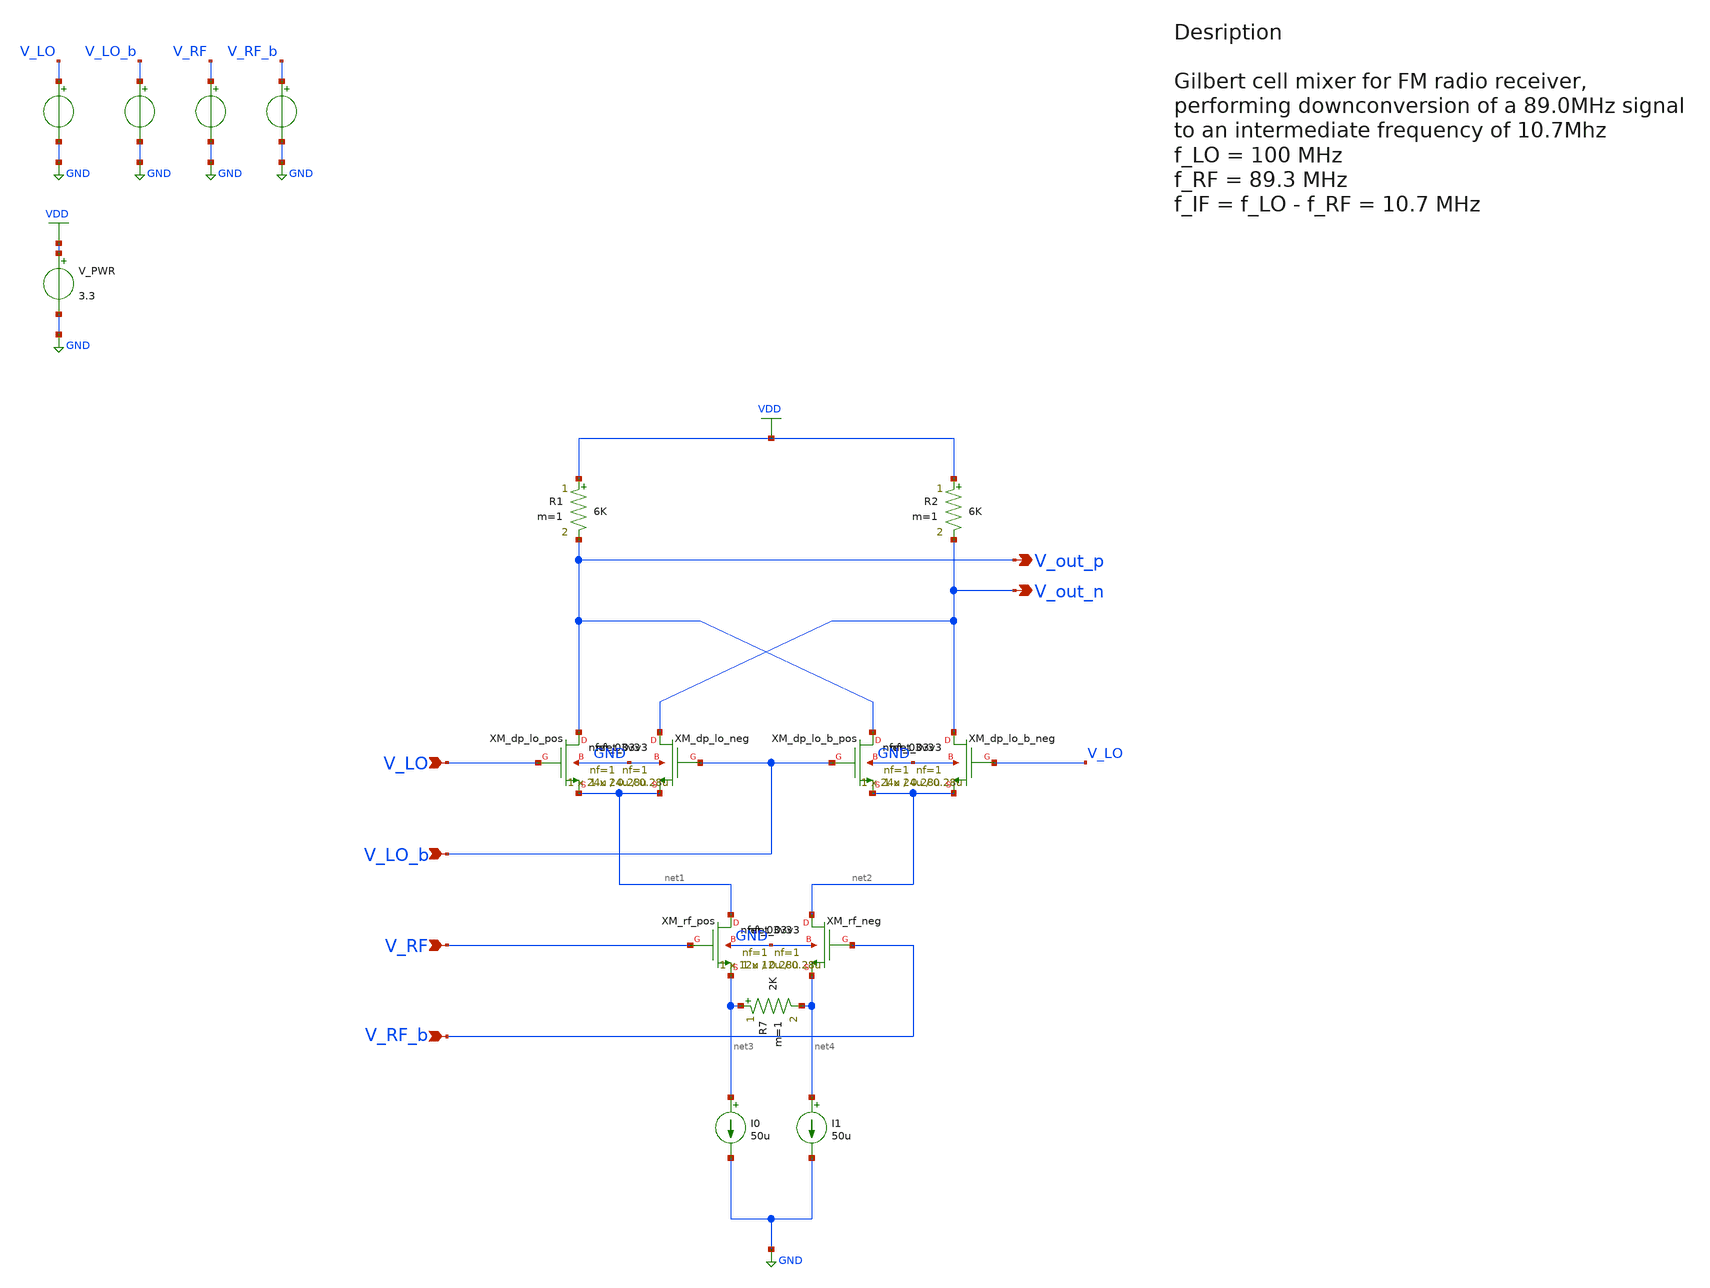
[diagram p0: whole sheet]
** sch_path: src/design_xsch/Gilbert_cell_no_hierarchy.sch
**.subckt Gilbert_cell_no_hierarchy V_LO V_LO_b V_RF V_RF_b V_out_p V_out_n
*.ipin V_LO
*.ipin V_LO_b
*.ipin V_RF
*.ipin V_RF_b
*.opin V_out_p
*.opin V_out_n
R1 VDD V_out_p 6K m=1
R2 VDD V_out_n 6K m=1
V_PWR VDD GND 3.3
.save i(v_pwr)
V_LO V_LO GND pulse(0 1.5 0 1p 1p 0.25n 0.5n)
.save i(v_lo)
V_LO_b V_LO_b GND pulse(0 1.5 0 1p 1p 0.25n 0.5n)
.save i(v_lo_b)
V_RF V_RF GND sin( 1 1 1 0 )
.save i(v_rf)
V_RF_b V_RF_b GND sin( 1 1 1 0 0 180 )
.save i(v_rf_b)
I0 net3 GND 50u
I1 net4 GND 50u
XM_dp_lo_pos V_out_p V_LO net1 GND nfet_03v3 L=0.28u W=24u nf=1 ad='int((nf+1)/2) * W/nf * 0.18u' as='int((nf+2)/2) * W/nf * 0.18u'
+ pd='2*int((nf+1)/2) * (W/nf + 0.18u)' ps='2*int((nf+2)/2) * (W/nf + 0.18u)' nrd='0.18u / W' nrs='0.18u / W'
+ sa=0 sb=0 sd=0 m=1
XM_dp_lo_neg V_out_n V_LO_b net1 GND nfet_03v3 L=0.28u W=24u nf=1 ad='int((nf+1)/2) * W/nf * 0.18u' as='int((nf+2)/2) * W/nf * 0.18u'
+ pd='2*int((nf+1)/2) * (W/nf + 0.18u)' ps='2*int((nf+2)/2) * (W/nf + 0.18u)' nrd='0.18u / W' nrs='0.18u / W'
+ sa=0 sb=0 sd=0 m=1
XM_dp_lo_b_pos V_out_p V_LO_b net2 GND nfet_03v3 L=0.28u W=24u nf=1 ad='int((nf+1)/2) * W/nf * 0.18u'
+ as='int((nf+2)/2) * W/nf * 0.18u' pd='2*int((nf+1)/2) * (W/nf + 0.18u)' ps='2*int((nf+2)/2) * (W/nf + 0.18u)'
+ nrd='0.18u / W' nrs='0.18u / W' sa=0 sb=0 sd=0 m=1
XM_dp_lo_b_neg V_out_n V_LO net2 GND nfet_03v3 L=0.28u W=24u nf=1 ad='int((nf+1)/2) * W/nf * 0.18u' as='int((nf+2)/2) * W/nf * 0.18u'
+ pd='2*int((nf+1)/2) * (W/nf + 0.18u)' ps='2*int((nf+2)/2) * (W/nf + 0.18u)' nrd='0.18u / W' nrs='0.18u / W'
+ sa=0 sb=0 sd=0 m=1
XM_rf_pos net1 V_RF net3 GND nfet_03v3 L=0.28u W=12u nf=1 ad='int((nf+1)/2) * W/nf * 0.18u' as='int((nf+2)/2) * W/nf * 0.18u'
+ pd='2*int((nf+1)/2) * (W/nf + 0.18u)' ps='2*int((nf+2)/2) * (W/nf + 0.18u)' nrd='0.18u / W' nrs='0.18u / W'
+ sa=0 sb=0 sd=0 m=1
XM_rf_neg net2 V_RF_b net4 GND nfet_03v3 L=0.28u W=12u nf=1 ad='int((nf+1)/2) * W/nf * 0.18u' as='int((nf+2)/2) * W/nf * 0.18u'
+ pd='2*int((nf+1)/2) * (W/nf + 0.18u)' ps='2*int((nf+2)/2) * (W/nf + 0.18u)' nrd='0.18u / W' nrs='0.18u / W'
+ sa=0 sb=0 sd=0 m=1
R7 net3 net4 2K m=1
**** begin user architecture code

.include $::180MCU_MODELS/design.ngspice
.lib $::180MCU_MODELS/sm141064.ngspice typical
.lib $::180MCU_MODELS/sm141064.ngspice mimcap_typical
.lib $::180MCU_MODELS/sm141064.ngspice cap_mim
.lib $::180MCU_MODELS/sm141064.ngspice res_typical




* let sets vectors to a plot, while set sets a variable, globally accessible in .control
.control

    * Set frequency and amplitude variables to proper values from within the control sequence
    * sine-wave LO
    * set cm_lo = 0.5
    * set freq_lo = 2.50G
    * set amp_lo = 0.5
    * alter @V_LO[sin] = [ $cm_lo $amp_lo $freq_lo 0 ]
    * alter @V_LO_b[sin] = [ $cm_lo $amp_lo $freq_lo 0 0 180 ]

    set freq_lo = 100Meg
    set cm_lo = 1.8
    set amp_lo = 0.25

    set cm_rf  = 1,6
    set freq_rf = 89.3Meg
    set amp_rf  = 0.2

    * set the parameters to the voltage sources
    * alter @V_LO[pulse] = [ 2 2.5 0 0.5p 0.5p 5n 10n ]
    * alter @V_LO_b[pulse] = [ 2 2.5 5n 0.5p 0.5p 5n 10n]
    alter @V_LO[sin] = [ $cm_lo $amp_lo $freq_lo 0 ]
    alter @V_LO_b[sin] = [ $cm_lo $amp_lo $freq_lo 0 0 180 ]
    alter @V_RF[sin] = [ $cm_rf $amp_rf $freq_rf 0 ]
    alter @V_RF_b[sin] = [ $cm_rf $amp_rf $freq_rf 0 0 180 ]

    save all

    * operating point
    op
    show

    * save transistor op parameters
    * diff_pair_1 transistors
    save @m.xm_rf_pos.m0[vgs]
    save @m.xm_rf_pos.m0[vds]
    save @m.xm_rf_pos.m0[id]
    save @m.xm_rf_pos.m0[gm]
    save @m.xm_rf_pos.m0[vth]
    save @m.xm_rf_pos.m0[cgg]
    save @m.xm_rf_neg.m0[vgs]
    save @m.xm_rf_neg.m0[vds]
    save @m.xm_rf_neg.m0[id]
    save @m.xm_rf_neg.m0[gm]
    save @m.xm_rf_neg.m0[vth]
    save @m.xm_rf_neg.m0[cgg]

    * diff_pair_2 transistors
    * save @m.xdiff_pair_2.xm1.m0[vgs]
    * save @m.xdiff_pair_2.xm1.m0[vds]
    * save @m.xdiff_pair_2.xm1.m0[id]
    * save @m.xdiff_pair_2.xm1.m0[gm]
    * save @m.xdiff_pair_2.xm1.m0[vth]
    * save @m.xdiff_pair_2.xm1.m0[cgg]
    * save @m.xdiff_pair_2.xm2.m0[vgs]
    * save @m.xdiff_pair_2.xm2.m0[vds]
    * save @m.xdiff_pair_2.xm2.m0[id]
    * save @m.xdiff_pair_2.xm2.m0[gm]
    * save @m.xdiff_pair_2.xm2.m0[vth]
    * save @m.xdiff_pair_2.xm2.m0[cgg]

    * diff_pair_3 transistors
    * save @m.xdiff_pair_3.xm1.m0[vgs]
    * save @m.xdiff_pair_3.xm1.m0[vds]
    * save @m.xdiff_pair_3.xm1.m0[id]
    * save @m.xdiff_pair_3.xm1.m0[gm]
    * save @m.xdiff_pair_3.xm1.m0[vth]
    * save @m.xdiff_pair_3.xm1.m0[cgg]
    * save @m.xdiff_pair_3.xm2.m0[vgs]
    * save @m.xdiff_pair_3.xm2.m0[vds]
    * save @m.xdiff_pair_3.xm2.m0[id]
    * save @m.xdiff_pair_3.xm2.m0[gm]
    * save @m.xdiff_pair_3.xm2.m0[vth]
    * save @m.xdiff_pair_3.xm2.m0[cgg]

    write Gilbert_no_hierarchy_sim.raw

    set appendwrite

    * Transient analysis to observe mixing operation
    tran 1p 300n
    write Gilbert_no_hierarchy_sim.raw

    * Calculate differential output for conversion gain measurement
    let v_out_diff = v(v_out_p)-v(v_out_n)
    let v_rf_diff = v(v_rf)-v(v_rf_b)

    * Extract IF component at 100MHz using FFT
    linearize v_out_diff v_rf_diff
    let time_step = 10e-12
    let sample_freq = 1/time_step
    let npts = length(v_out_diff)
    let freq_res = sample_freq/npts


    fft v_out_diff v_rf_diff
    * Find frequency bins

    * print everything, sanity check
    * set     ; print all available global (?) variables (?)
    * setplot ; print all plots
    * display ; print variables available in current plot

    let freq_res = tran2.freq_res
    let freq_if = abs( $freq_lo - $freq_rf )

    let if_bin = floor( freq_if/freq_res )
    let rf_bin = floor( $freq_rf/freq_res )

    * Measure conversion gain (power gain from RF to IF)
    let rf_mag = abs(v_rf_diff[rf_bin])
    let if_mag = abs(v_out_diff[if_bin])
    let conversion_gain_db = 20*log10(if_mag/rf_mag)
    print conversion_gain_db

    write Gilbert_no_hierarchy_sim.raw

.endc


**** end user architecture code
**.ends
.GLOBAL VDD
.GLOBAL GND
.end
